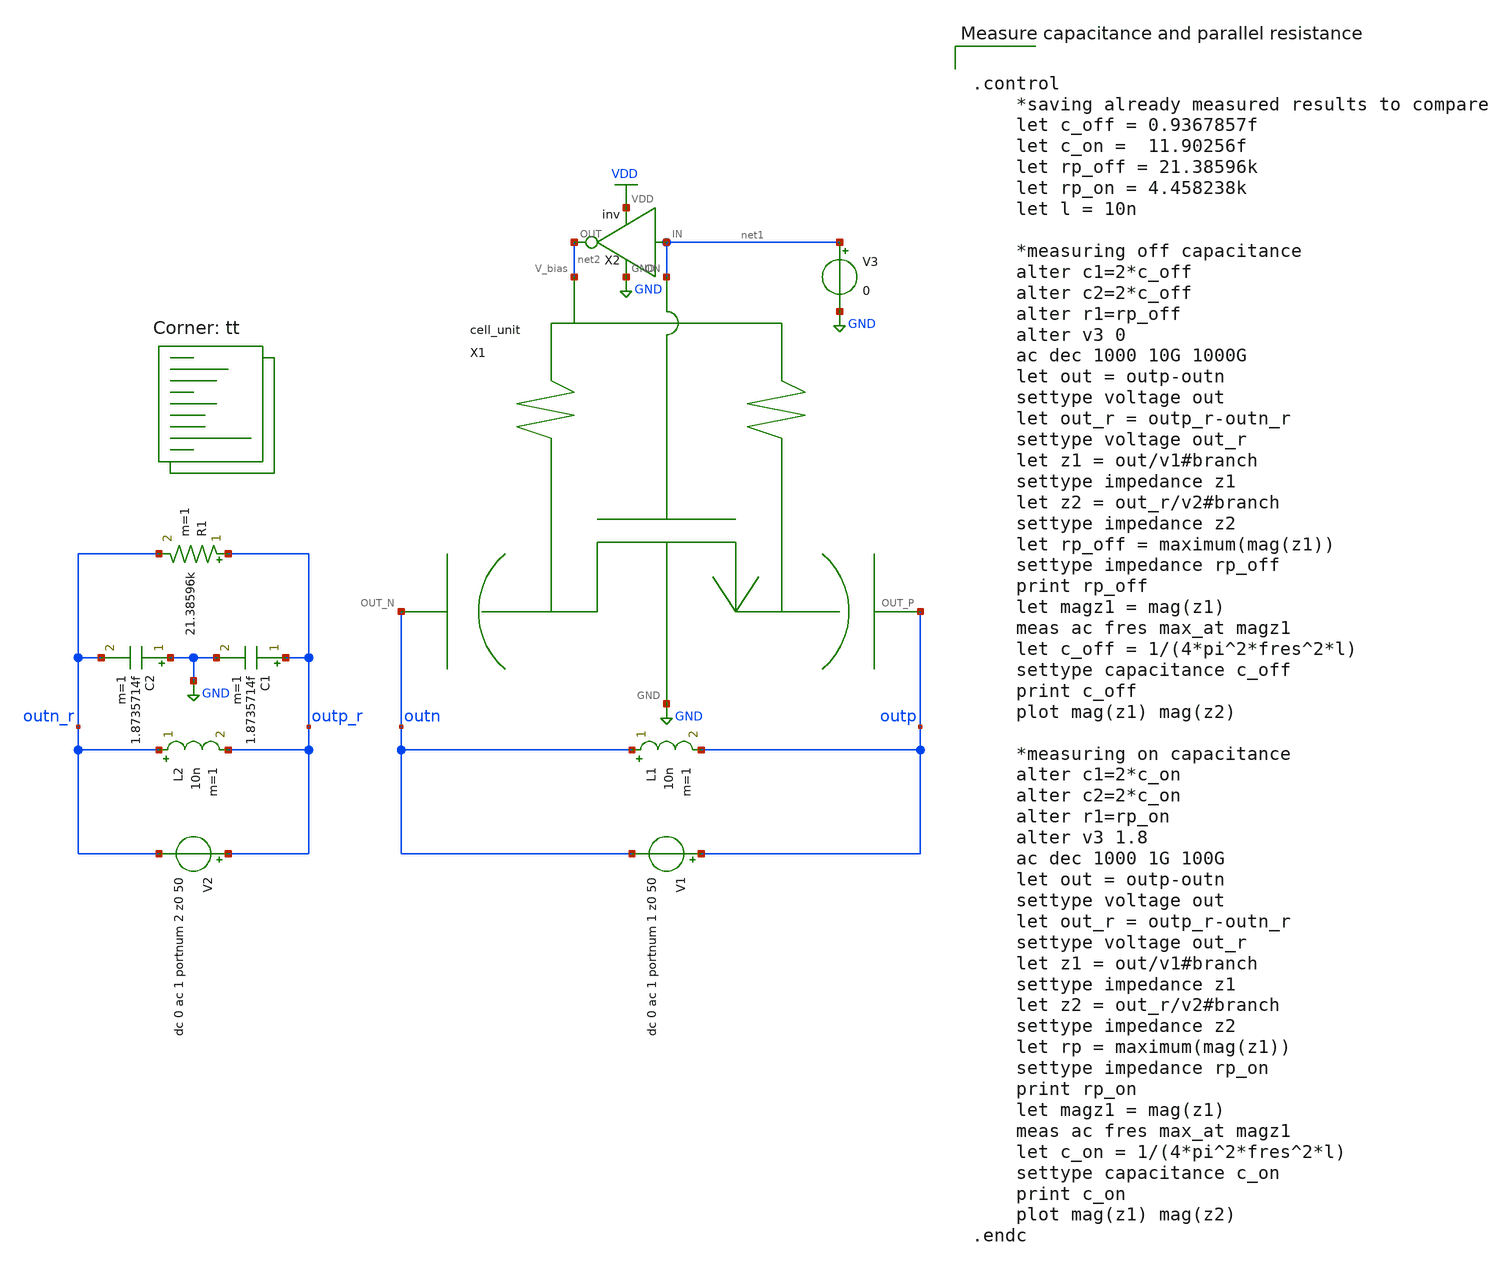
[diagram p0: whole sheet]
** sch_path: xschem/vco/testbenches/capbank/cell_unit_capacity_measurement_tb.sch
**.subckt cell_unit_capacity_measurement_tb
X1 net2 net1 outn GND outp cell_unit
X2 net1 net2 VDD GND inv
V3 net1 GND 0
V1 outp outn dc 0 ac 1 portnum 1 z0 50
L1 outn outp 10n m=1
V2 outp_r outn_r dc 0 ac 1 portnum 2 z0 50
L2 outn_r outp_r 10n m=1
C1 outp_r GND 1.8735714f m=1
C2 GND outn_r 1.8735714f m=1
R1 outp_r outn_r 21.38596k m=1
**** begin user architecture code
.lib $::SKYWATER_MODELS/sky130.lib.spice tt


.control
    *saving already measured results to compare
    let c_off = 0.9367857f
    let c_on =  11.90256f
    let rp_off = 21.38596k
    let rp_on = 4.458238k
    let l = 10n

    *measuring off capacitance
    alter c1=2*c_off
    alter c2=2*c_off
    alter r1=rp_off
    alter v3 0
    ac dec 1000 10G 1000G
    let out = outp-outn
    settype voltage out
    let out_r = outp_r-outn_r
    settype voltage out_r
    let z1 = out/v1#branch
    settype impedance z1
    let z2 = out_r/v2#branch
    settype impedance z2
    let rp_off = maximum(mag(z1))
    settype impedance rp_off
    print rp_off
    let magz1 = mag(z1)
    meas ac fres max_at magz1
    let c_off = 1/(4*pi^2*fres^2*l)
    settype capacitance c_off
    print c_off
    plot mag(z1) mag(z2)

    *measuring on capacitance
    alter c1=2*c_on
    alter c2=2*c_on
    alter r1=rp_on
    alter v3 1.8
    ac dec 1000 1G 100G
    let out = outp-outn
    settype voltage out
    let out_r = outp_r-outn_r
    settype voltage out_r
    let z1 = out/v1#branch
    settype impedance z1
    let z2 = out_r/v2#branch
    settype impedance z2
    let rp = maximum(mag(z1))
    settype impedance rp_on
    print rp_on
    let magz1 = mag(z1)
    meas ac fres max_at magz1
    let c_on = 1/(4*pi^2*fres^2*l)
    settype capacitance c_on
    print c_on
    plot mag(z1) mag(z2)
.endc


**** end user architecture code
**.ends
.GLOBAL GND
.GLOBAL VDD
.end
